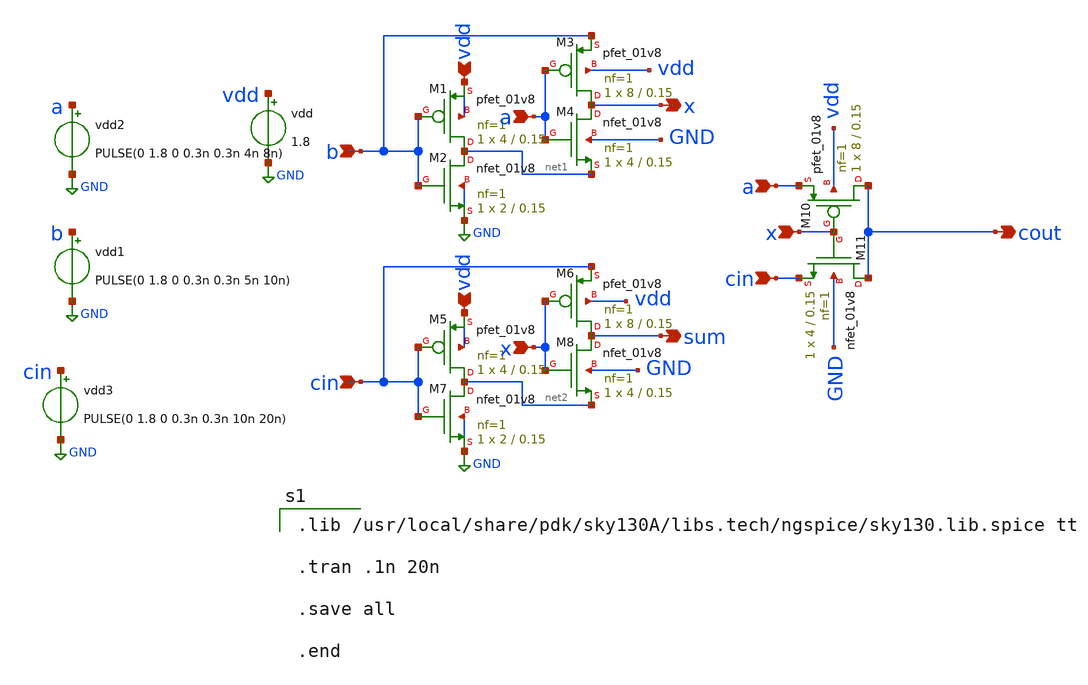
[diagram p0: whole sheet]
** sch_path: Circuit/circuit.sch
**.subckt circuit b x a vdd cin sum x vdd a cin x cout
*.ipin b
*.opin x
*.ipin a
*.ipin vdd
*.ipin cin
*.opin sum
*.ipin x
*.ipin vdd
*.ipin a
*.ipin cin
*.ipin x
*.opin cout
XM1 net1 b vdd vdd sky130_fd_pr__pfet_01v8 L=0.15 W=4 nf=1 ad='int((nf+1)/2) * W/nf * 0.29' as='int((nf+2)/2) * W/nf * 0.29'
+ pd='2*int((nf+1)/2) * (W/nf + 0.29)' ps='2*int((nf+2)/2) * (W/nf + 0.29)' nrd='0.29 / W' nrs='0.29 / W'
+ sa=0 sb=0 sd=0 mult=1 m=1
XM3 x a b vdd sky130_fd_pr__pfet_01v8 L=0.15 W=8 nf=1 ad='int((nf+1)/2) * W/nf * 0.29' as='int((nf+2)/2) * W/nf * 0.29'
+ pd='2*int((nf+1)/2) * (W/nf + 0.29)' ps='2*int((nf+2)/2) * (W/nf + 0.29)' nrd='0.29 / W' nrs='0.29 / W'
+ sa=0 sb=0 sd=0 mult=1 m=1
XM2 net1 b GND GND sky130_fd_pr__nfet_01v8 L=0.15 W=2 nf=1 ad='int((nf+1)/2) * W/nf * 0.29' as='int((nf+2)/2) * W/nf * 0.29'
+ pd='2*int((nf+1)/2) * (W/nf + 0.29)' ps='2*int((nf+2)/2) * (W/nf + 0.29)' nrd='0.29 / W' nrs='0.29 / W'
+ sa=0 sb=0 sd=0 mult=1 m=1
XM4 x a net1 GND sky130_fd_pr__nfet_01v8 L=0.15 W=4 nf=1 ad='int((nf+1)/2) * W/nf * 0.29' as='int((nf+2)/2) * W/nf * 0.29'
+ pd='2*int((nf+1)/2) * (W/nf + 0.29)' ps='2*int((nf+2)/2) * (W/nf + 0.29)' nrd='0.29 / W' nrs='0.29 / W'
+ sa=0 sb=0 sd=0 mult=1 m=1
vdd vdd GND 1.8
.save i(vdd)
vdd1 b GND PULSE(0 1.8 0 0.3n 0.3n 5n 10n)
.save i(vdd1)
vdd2 a GND PULSE(0 1.8 0 0.3n 0.3n 4n 8n)
.save i(vdd2)
XM5 net2 cin vdd vdd sky130_fd_pr__pfet_01v8 L=0.15 W=4 nf=1 ad='int((nf+1)/2) * W/nf * 0.29' as='int((nf+2)/2) * W/nf * 0.29'
+ pd='2*int((nf+1)/2) * (W/nf + 0.29)' ps='2*int((nf+2)/2) * (W/nf + 0.29)' nrd='0.29 / W' nrs='0.29 / W'
+ sa=0 sb=0 sd=0 mult=1 m=1
XM6 sum x cin vdd sky130_fd_pr__pfet_01v8 L=0.15 W=8 nf=1 ad='int((nf+1)/2) * W/nf * 0.29' as='int((nf+2)/2) * W/nf * 0.29'
+ pd='2*int((nf+1)/2) * (W/nf + 0.29)' ps='2*int((nf+2)/2) * (W/nf + 0.29)' nrd='0.29 / W' nrs='0.29 / W'
+ sa=0 sb=0 sd=0 mult=1 m=1
XM7 net2 cin GND GND sky130_fd_pr__nfet_01v8 L=0.15 W=2 nf=1 ad='int((nf+1)/2) * W/nf * 0.29' as='int((nf+2)/2) * W/nf * 0.29'
+ pd='2*int((nf+1)/2) * (W/nf + 0.29)' ps='2*int((nf+2)/2) * (W/nf + 0.29)' nrd='0.29 / W' nrs='0.29 / W'
+ sa=0 sb=0 sd=0 mult=1 m=1
XM8 sum x net2 GND sky130_fd_pr__nfet_01v8 L=0.15 W=4 nf=1 ad='int((nf+1)/2) * W/nf * 0.29' as='int((nf+2)/2) * W/nf * 0.29'
+ pd='2*int((nf+1)/2) * (W/nf + 0.29)' ps='2*int((nf+2)/2) * (W/nf + 0.29)' nrd='0.29 / W' nrs='0.29 / W'
+ sa=0 sb=0 sd=0 mult=1 m=1
vdd3 cin GND PULSE(0 1.8 0 0.3n 0.3n 10n 20n)
.save i(vdd3)
XM10 cout x a vdd sky130_fd_pr__pfet_01v8 L=0.15 W=8 nf=1 ad='int((nf+1)/2) * W/nf * 0.29' as='int((nf+2)/2) * W/nf * 0.29'
+ pd='2*int((nf+1)/2) * (W/nf + 0.29)' ps='2*int((nf+2)/2) * (W/nf + 0.29)' nrd='0.29 / W' nrs='0.29 / W'
+ sa=0 sb=0 sd=0 mult=1 m=1
XM11 cout x cin GND sky130_fd_pr__nfet_01v8 L=0.15 W=4 nf=1 ad='int((nf+1)/2) * W/nf * 0.29' as='int((nf+2)/2) * W/nf * 0.29'
+ pd='2*int((nf+1)/2) * (W/nf + 0.29)' ps='2*int((nf+2)/2) * (W/nf + 0.29)' nrd='0.29 / W' nrs='0.29 / W'
+ sa=0 sb=0 sd=0 mult=1 m=1
**** begin user architecture code

.lib /usr/local/share/pdk/sky130A/libs.tech/ngspice/sky130.lib.spice tt

.tran .1n 20n

.save all

.end

**** end user architecture code
**.ends
.GLOBAL GND
.end
